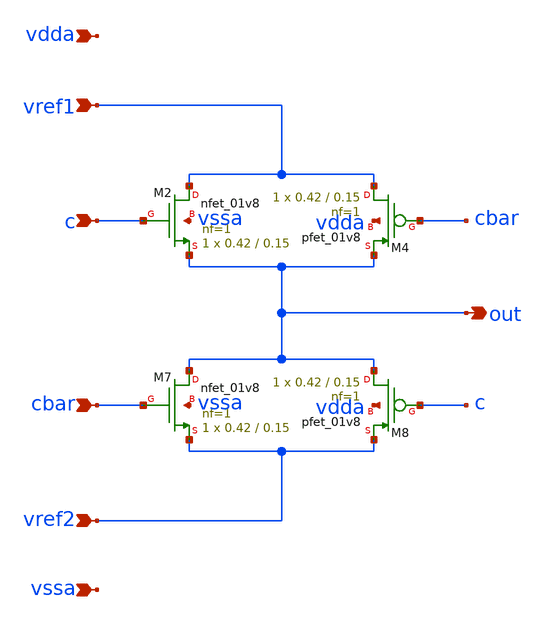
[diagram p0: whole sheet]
** sch_path: xschem/mux/analogMux.sch
**.subckt analogMux vref1 out vref2 c cbar vssa vdda
*.ipin vref1
*.opin out
*.ipin vref2
*.ipin c
*.ipin cbar
*.ipin vssa
*.ipin vdda
XM2 vref1 c out vssa sky130_fd_pr__nfet_01v8 L=0.15 W=0.42 nf=1 ad='int((nf+1)/2) * W/nf * 0.29' as='int((nf+2)/2) * W/nf * 0.29'
+ pd='2*int((nf+1)/2) * (W/nf + 0.29)' ps='2*int((nf+2)/2) * (W/nf + 0.29)' nrd='0.29 / W' nrs='0.29 / W'
+ sa=0 sb=0 sd=0 mult=1 m=1
XM4 vref1 cbar out vdda sky130_fd_pr__pfet_01v8 L=0.15 W=0.42 nf=1 ad='int((nf+1)/2) * W/nf * 0.29' as='int((nf+2)/2) * W/nf * 0.29'
+ pd='2*int((nf+1)/2) * (W/nf + 0.29)' ps='2*int((nf+2)/2) * (W/nf + 0.29)' nrd='0.29 / W' nrs='0.29 / W'
+ sa=0 sb=0 sd=0 mult=1 m=1
XM7 out cbar vref2 vssa sky130_fd_pr__nfet_01v8 L=0.15 W=0.42 nf=1 ad='int((nf+1)/2) * W/nf * 0.29' as='int((nf+2)/2) * W/nf * 0.29'
+ pd='2*int((nf+1)/2) * (W/nf + 0.29)' ps='2*int((nf+2)/2) * (W/nf + 0.29)' nrd='0.29 / W' nrs='0.29 / W'
+ sa=0 sb=0 sd=0 mult=1 m=1
XM8 out c vref2 vdda sky130_fd_pr__pfet_01v8 L=0.15 W=0.42 nf=1 ad='int((nf+1)/2) * W/nf * 0.29' as='int((nf+2)/2) * W/nf * 0.29'
+ pd='2*int((nf+1)/2) * (W/nf + 0.29)' ps='2*int((nf+2)/2) * (W/nf + 0.29)' nrd='0.29 / W' nrs='0.29 / W'
+ sa=0 sb=0 sd=0 mult=1 m=1
**.ends
.end
